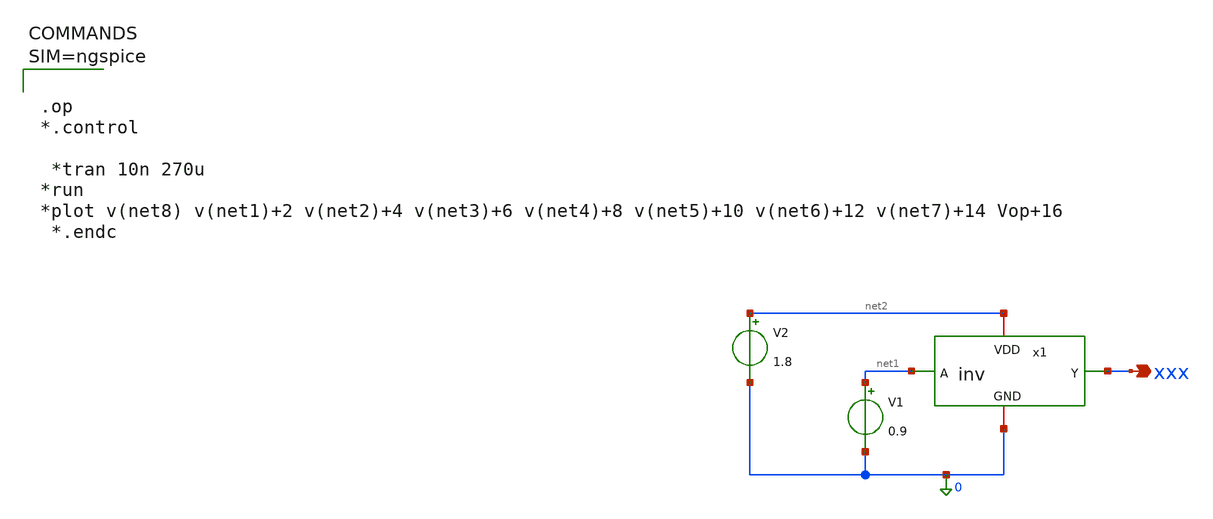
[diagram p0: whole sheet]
** sch_path: sar-adc/untitled.sch
**.subckt untitled xxx
*.opin xxx
x1 net2 net1 xxx 0 inv
V1 net1 0 0.9
V2 net2 0 1.8
**** begin user architecture code



.op
*.control

 *tran 10n 270u
*run
*plot v(net8) v(net1)+2 v(net2)+4 v(net3)+6 v(net4)+8 v(net5)+10 v(net6)+12 v(net7)+14 Vop+16
 *.endc




** opencircuitdesign pdks install
.lib $::SKYWATER_MODELS/sky130.lib.spice tt

**** end user architecture code
**.ends

* expanding   symbol:  inv.sym # of pins=4
** sym_path: sar-adc/inv.sym
** sch_path: sar-adc/inv.sch
.subckt inv VDD A Y GND
*.iopin GND
*.iopin VDD
*.ipin A
*.opin Y
XM1 Y A GND GND sky130_fd_pr__nfet_01v8 L=0.65 W=1 nf=1 ad='int((1 + 1)/2) * 1 / 1 * 0.29' as='int((1 + 2)/2) * 1 / 1 * 0.29'
+ pd='2*int((1 + 1)/2) * (1 / 1 + 0.29)' ps='2*int((1 + 2)/2) * (1 / 1 + 0.29)' nrd='0.29 / 1 ' nrs='0.29 / 1 '
+ sa=0 sb=0 sd=0 mult=1 m=1
XM2 Y A VDD VDD sky130_fd_pr__pfet_01v8 L=0.15 W=1 nf=1 ad='int((1 + 1)/2) * 1 / 1 * 0.29' as='int((1 + 2)/2) * 1 / 1 * 0.29'
+ pd='2*int((1 + 1)/2) * (1 / 1 + 0.29)' ps='2*int((1 + 2)/2) * (1 / 1 + 0.29)' nrd='0.29 / 1 ' nrs='0.29 / 1 '
+ sa=0 sb=0 sd=0 mult=1 m=1
.ends

.end
